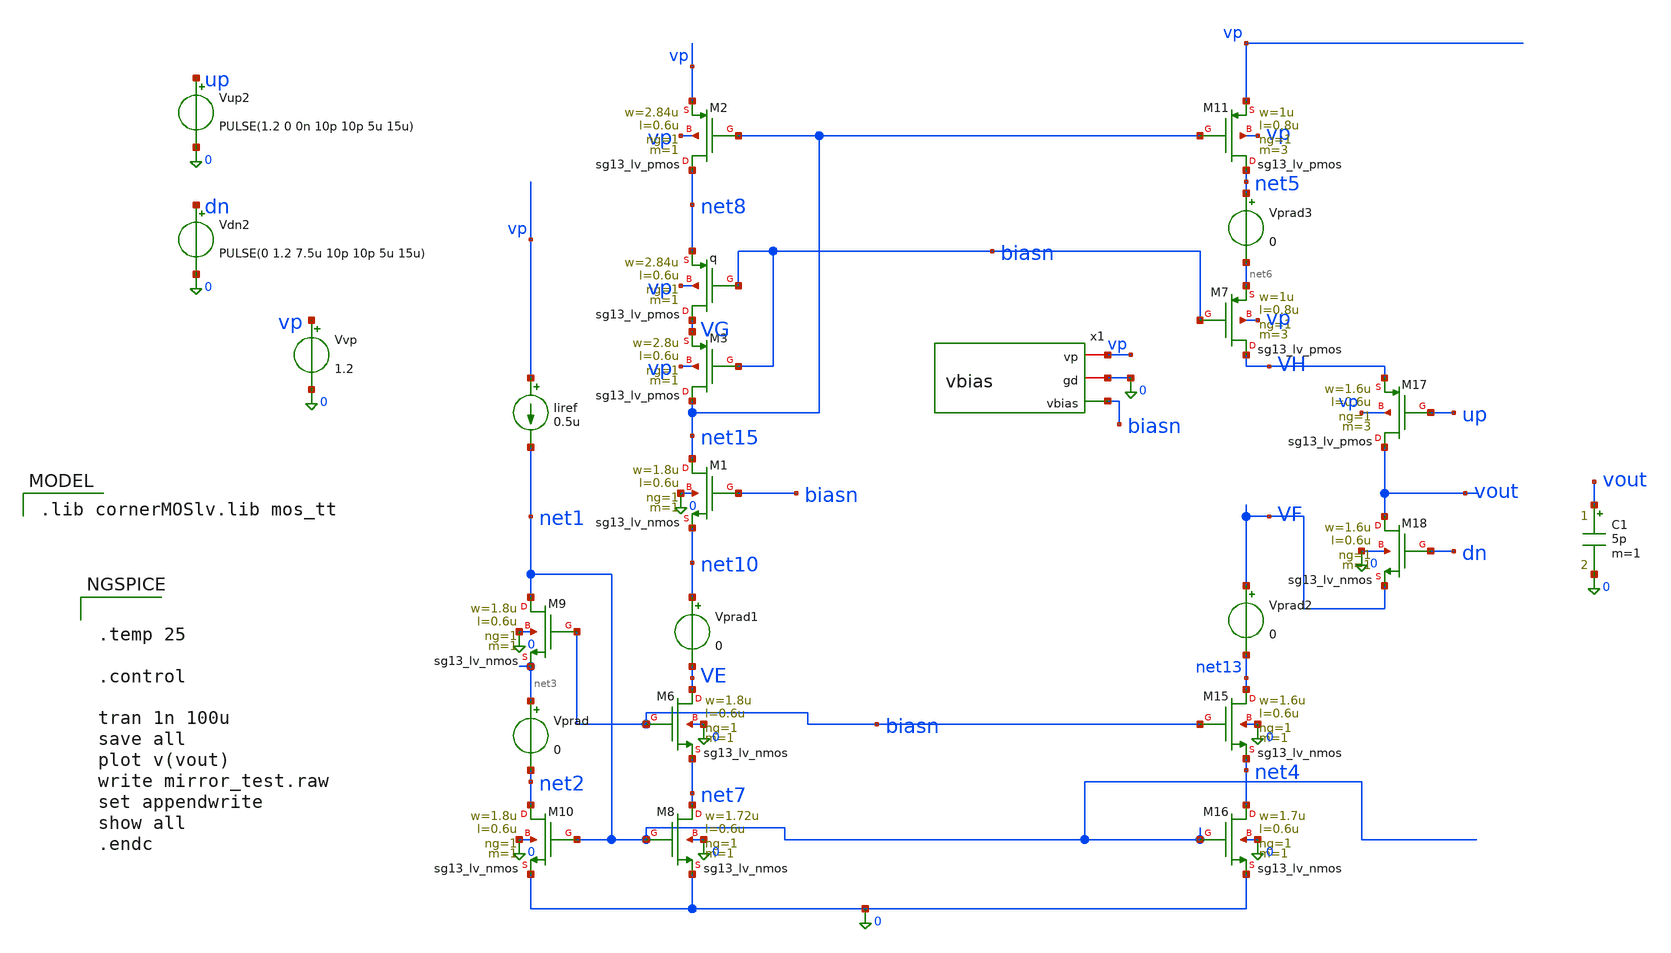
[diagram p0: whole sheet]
** sch_path: PLL0663-main/schematic/xschem/charge_pump/old_sch/mirror_test_tb.sch
**.subckt mirror_test_tb
XM15 net13 biasn net4 0 sg13_lv_nmos w=1.6u l=0.6u ng=1 m=1 mm_ok=1
XM16 net4 net1 0 0 sg13_lv_nmos w=1.7u l=0.6u ng=1 m=1 mm_ok=1
XM1 net15 biasn net10 0 sg13_lv_nmos w=1.8u l=0.6u ng=1 m=1 mm_ok=1
XM6 VE biasn net7 0 sg13_lv_nmos w=1.8u l=0.6u ng=1 m=1 mm_ok=1
XM8 net7 net1 0 0 sg13_lv_nmos w=1.72u l=0.6u ng=1 m=1 mm_ok=1
XM9 net1 biasn net3 0 sg13_lv_nmos w=1.8u l=0.6u ng=1 m=1 mm_ok=1
XM10 net2 net1 0 0 sg13_lv_nmos w=1.8u l=0.6u ng=1 m=1 mm_ok=1
Vvp vp 0 1.2
Iiref vp net1 0.5u
Vprad net3 net2 0
Vprad1 net10 VE 0
Vprad2 VF net13 0
Xq VG biasn net8 vp sg13_lv_pmos w=2.84u l=0.6u ng=1 m=1 mm_ok=1
XM3 net15 biasn VG vp sg13_lv_pmos w=2.8u l=0.6u ng=1 m=1 mm_ok=1
XM7 VH biasn net6 vp sg13_lv_pmos w=1u l=0.8u ng=1 m=3 mm_ok=1
XM11 net5 net15 vp vp sg13_lv_pmos w=1u l=0.8u ng=1 m=3 mm_ok=1
Vprad3 net5 net6 0
XM2 net8 net15 vp vp sg13_lv_pmos w=2.84u l=0.6u ng=1 m=1 mm_ok=1
XM17 vout up VH vp sg13_lv_pmos w=1.6u l=0.6u ng=1 m=3 mm_ok=1
XM18 vout dn VF 0 sg13_lv_nmos w=1.6u l=0.6u ng=1 m=1 mm_ok=1
C1 vout 0 5p m=1
x1 vp 0 biasn vbias
Vup2 up 0 PULSE(1.2 0 0n 10p 10p 5u 15u)
Vdn2 dn 0 PULSE(0 1.2 7.5u 10p 10p 5u 15u)
**** begin user architecture code
 .lib cornerMOSlv.lib mos_tt



.temp 25

.control

tran 1n 100u
save all
plot v(vout)
write mirror_test.raw
set appendwrite
show all
.endc


**** end user architecture code
**.ends

* expanding   symbol:
*+  /foss/designs/IHP__PLL0663/PLL0663-main/schematic/xschem/charge_pump/vbias.sym # of pins=3
** sym_path: /foss/designs/IHP__PLL0663/PLL0663-main/schematic/xschem/charge_pump/vbias.sym
** sch_path: /foss/designs/IHP__PLL0663/PLL0663-main/schematic/xschem/charge_pump/vbias.sch
.subckt vbias vp gd vbias
*.opin vbias
*.iopin gd
*.iopin vp
XM5 net1 iref vp vp sg13_lv_pmos w=1.2u l=0.6u ng=1 m=1 mm_ok=1
XM6 vbias net1 net2 gd sg13_lv_nmos w=3.6u l=0.6u ng=1 m=1 mm_ok=1
XM2 net2 net2 gd gd sg13_lv_nmos w=1.2u l=0.6u ng=1 m=1 mm_ok=1
XM3 gd gd gd gd sg13_lv_nmos w=1.86u l=0.6u ng=1 m=1 mm_ok=1
XM7 vp vp vp vp sg13_lv_pmos w=1.375u l=0.6u ng=1 m=1 mm_ok=1
XR1 net1 vbias gd rppd w=1e-6 l=1.7e-6 m=1 b=0 mm_ok=1
x1 vp iref gd curr_source
.ends


* expanding   symbol:
*+  /foss/designs/IHP__PLL0663/PLL0663-main/schematic/xschem/charge_pump/curr_source.sym # of pins=3
** sym_path: /foss/designs/IHP__PLL0663/PLL0663-main/schematic/xschem/charge_pump/curr_source.sym
** sch_path: /foss/designs/IHP__PLL0663/PLL0663-main/schematic/xschem/charge_pump/curr_source.sch
.subckt curr_source vp iref gd
*.iopin vp
*.iopin gd
*.opin iref
XM9 net3 net3 gd gd sg13_lv_nmos w=1u l=0.6u ng=1 m=1 mm_ok=1
XM4 iref iref vp vp sg13_lv_pmos w=1.4u l=0.6u ng=1 m=1 mm_ok=1
XM5 net2 iref vp vp sg13_lv_pmos w=1.2u l=0.6u ng=1 m=1 mm_ok=1
XM10 iref net2 net1 gd sg13_lv_nmos w=1.2u l=0.6u ng=1 m=1 mm_ok=1
XM1 net2 net2 gd gd sg13_lv_nmos w=1.4u l=0.6u ng=1 m=1 mm_ok=1
XM3 vp vp net3 gd sg13_lv_nmos w=1u l=0.6u ng=1 m=1 mm_ok=1
XM6 vp net3 iref gd sg13_lv_nmos w=1u l=0.6u ng=1 m=1 mm_ok=1
XM2 gd gd gd gd sg13_lv_nmos w=0.4u l=0.6u ng=1 m=1 mm_ok=1
XR2 net1 gd gd rppd w=1e-6 l=1.7e-6 m=1 b=0 mm_ok=1
.ends

.end
